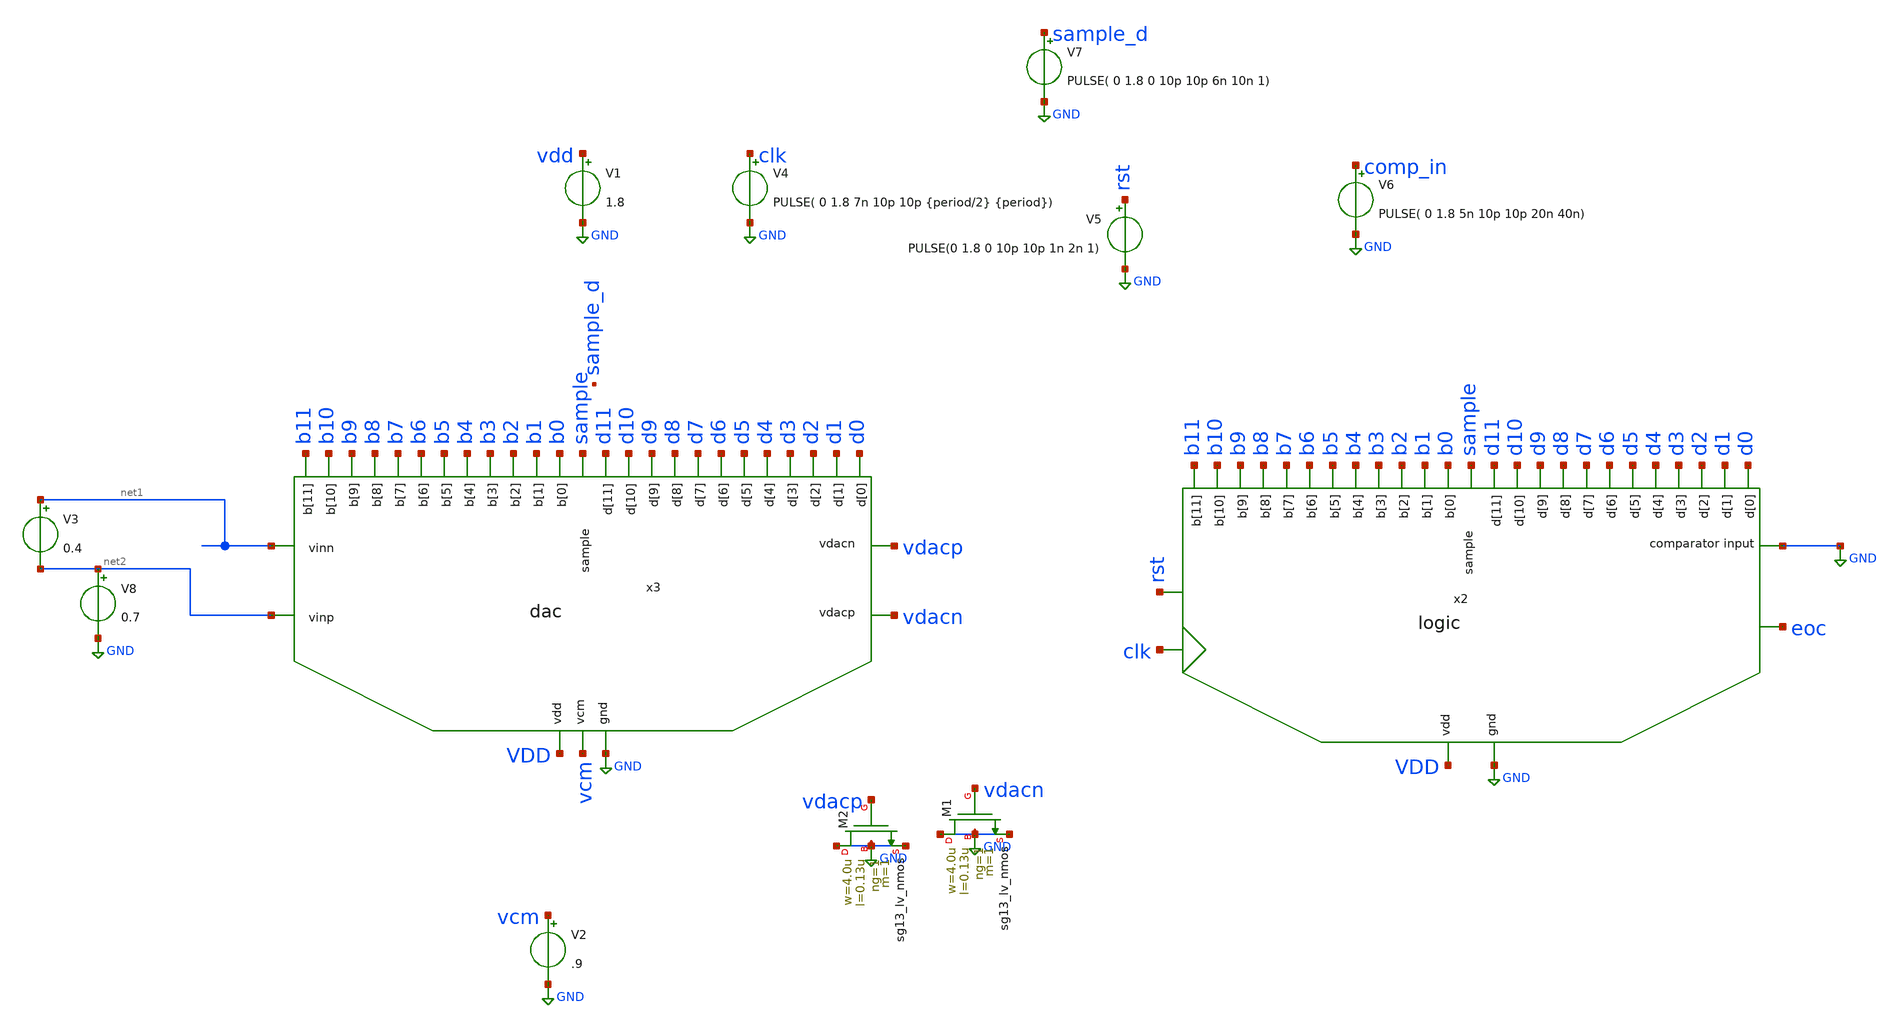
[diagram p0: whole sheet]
** sch_path: xschem/dac_icms_cell_ideall/testbenches/tb_dac.sch
**.subckt tb_dac
x3 vdacp vcm b9 b7 b0 b11 b3 b4 b2 b1 b8 b6 b5 b10 GND VDD sample vdacn net2 net1 d9 d7 d0 d11 d3 d4
+ d2 d1 d8 d6 d5 d10 dac cu=10f
V1 vdd GND 1.8
V2 vcm GND .9
x2 b9 b7 b0 b11 b3 b4 b2 b1 b8 b6 b5 b10 GND VDD sample d9 d7 d0 d11 d3 d4 d2 d1 d8 d6 d5 d10 GND
+ clk rst eoc logic
V3 net1 net2 0.4
V4 clk GND PULSE( 0 1.8 7n 10p 10p {period/2} {period})
V6 comp_in GND PULSE( 0 1.8 5n 10p 10p 20n 40n)
V7 sample_d GND PULSE( 0 1.8 0 10p 10p 6n 10n 1)
V5 rst GND PULSE(0 1.8 0 10p 10p 1n 2n 1)
XM2 GND vdacp GND GND sg13_lv_nmos w=4.0u l=0.13u ng=1 m=1 mm_ok=1
XM1 GND vdacn GND GND sg13_lv_nmos w=4.0u l=0.13u ng=1 m=1 mm_ok=1
V8 net2 GND 0.7
**** begin user architecture code


.param temp=27
.param period = 5n
.param stop={20*period}
.param ro = 500
.param W_P = 1.0u
.param L_P = 0.13u
.param W_N = 1.0u
.param L_N = 0.13u
.options savecurrents klu method=gear reltol=1e-2 abstol=1e-15 gmin=1e-10
.control

* Transient Analysis
tran 100p 50n

plot {d0} {d1 + 4} {d2 + 8} {d3 + 12} {d4 + 16} {d5 + 20} {d6 + 24} {d7 + 28} {d8 + 32} {d9 + 36} {d10 + 40}
+ {d11 + 44}
plot {b0} {b1 + 4} {b2 + 8} {b3 + 12} {b4 + 16} {b5 + 20} {b6 + 24} {b7 + 28} {b8 + 32} {b9 + 36} {b10 + 40}
+ {b11 + 44}
plot {clk} {comp_in + 2} {sample + 4}
plot vdacp vdacn
plot {vdacp-vdacn}

.endc




** IHP models
.lib cornerMOSlv.lib mos_tt
.lib cornerMOShv.lib mos_tt
.lib cornerHBT.lib hbt_typ
.lib cornerRES.lib res_typ
.include /foss/pdks/ihp-sg13g2/libs.ref/sg13g2_stdcell/spice/sg13g2_stdcell.spice


**** end user architecture code
**.ends
.GLOBAL GND
.end
